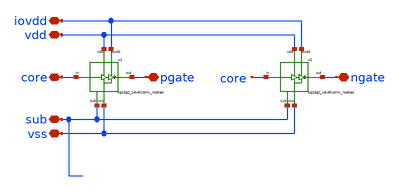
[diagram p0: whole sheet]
** sch_path: MSPHY6034-main/schematic/xschem/openpdk-libraries/ihp-sg13g2/sg13g2_io/xschem/sg13g2_GateLevelUpInv_noptap.sch
**.subckt sg13g2_GateLevelUpInv_noptap iovdd vss pgate core vdd sub ngate
*.iopin iovdd
*.iopin vss
*.iopin pgate
*.iopin core
*.iopin vdd
*.iopin sub
*.iopin ngate
x1 iovdd vss core pgate vdd sub sg13g2_LevelUpInv_noptap
x2 iovdd vss core ngate vdd sub sg13g2_LevelUpInv_noptap
**.ends

* expanding   symbol:  sg13g2_LevelUpInv_noptap.sym # of pins=6
** sym_path: MSPHY6034-main/schematic/xschem/openpdk-libraries/ihp-sg13g2/sg13g2_io/xschem/sg13g2_LevelUpInv_noptap.sym
** sch_path: MSPHY6034-main/schematic/xschem/openpdk-libraries/ihp-sg13g2/sg13g2_io/xschem/sg13g2_LevelUpInv_noptap.sch
.subckt sg13g2_LevelUpInv_noptap iovdd vss in out vdd sub
*.iopin iovdd
*.iopin vss
*.iopin out
*.iopin in
*.iopin vdd
*.iopin sub
XM1 net1 in vss sub sg13_hv_nmos w=1.9u l=0.45u ng=1 m=1 mm_ok=1
XM3 net1 net2 iovdd iovdd sg13_hv_pmos w=0.3u l=0.45u ng=1 m=1 mm_ok=1
XM4 net2 net1 iovdd iovdd sg13_hv_pmos w=0.3u l=0.45u ng=1 m=1 mm_ok=1
XM5 out net2 iovdd iovdd sg13_hv_pmos w=3.9u l=0.45u ng=1 m=1 mm_ok=1
XM2 net2 net3 vss sub sg13_hv_nmos w=1.9u l=0.45u ng=1 m=1 mm_ok=1
XM6 out net2 vss sub sg13_hv_nmos w=1.9u l=0.45u ng=1 m=1 mm_ok=1
XM7 net3 in vss sub sg13_lv_nmos w=2.75u l=0.13u ng=1 m=1 mm_ok=1
XM8 net3 in vdd vdd sg13_lv_pmos w=4.75u l=0.13u ng=1 m=1 mm_ok=1
.ends

.end
